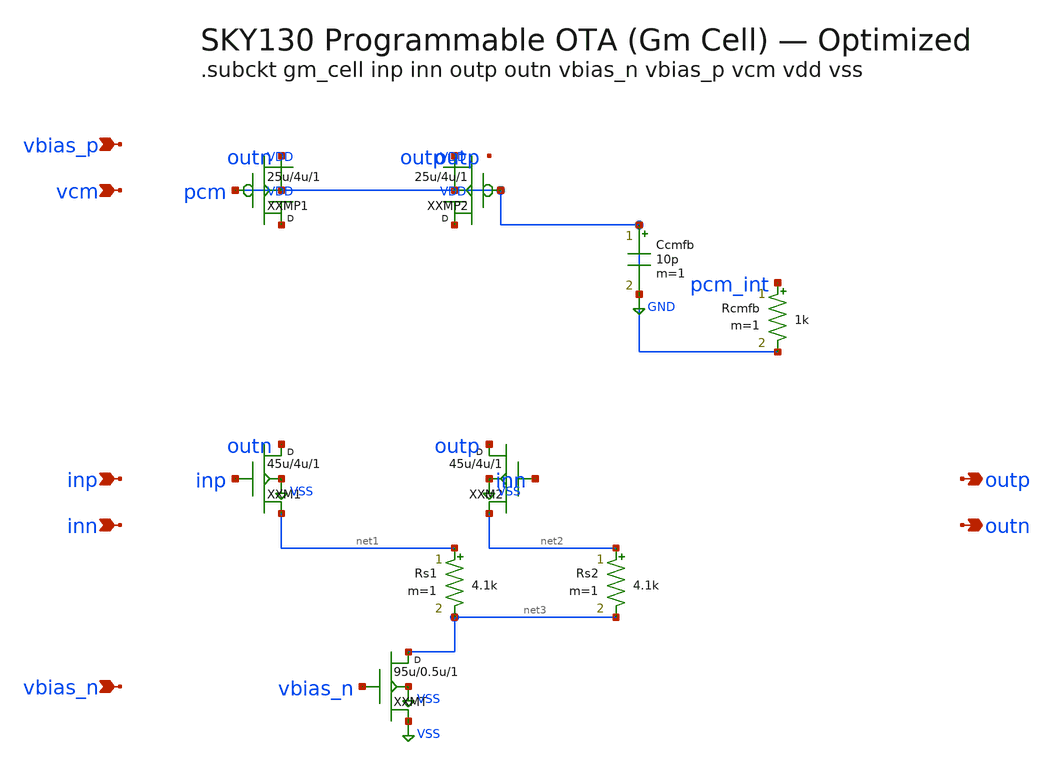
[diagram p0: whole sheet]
** sch_path: data/sch/ode_gm-cell.sch
**.subckt ode_gm-cell inp inn vbias_n vbias_p vcm outp outn
*.ipin inp
*.ipin inn
*.ipin vbias_n
*.ipin vbias_p
*.ipin vcm
*.opin outp
*.opin outn
XXM1 outn inp net1 VSS sky130_fd_pr__nfet_01v8 w=45u l=4u m=1
XXM2 outp inn net2 VSS sky130_fd_pr__nfet_01v8 w=45u l=4u m=1
Rs1 net1 net3 4.1k m=1
Rs2 net2 net3 4.1k m=1
XXMT net3 vbias_n VSS VSS sky130_fd_pr__nfet_01v8 w=95u l=0.5u m=1
XXMP1 VDD pcm outn pcm sky130_fd_pr__pfet_01v8 w=25u l=4u m=1
XXMP2 VDD pcm outp pcm sky130_fd_pr__pfet_01v8 w=25u l=4u m=1
Rcmfb pcm_int pcm 1k m=1
Ccmfb pcm pcm 10p m=1
**.ends
.GLOBAL VSS
.GLOBAL VDD
.GLOBAL GND
.end
